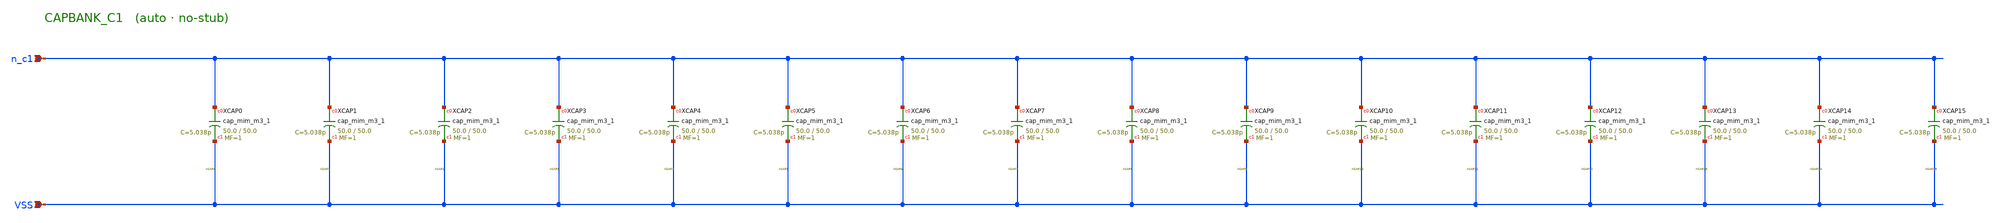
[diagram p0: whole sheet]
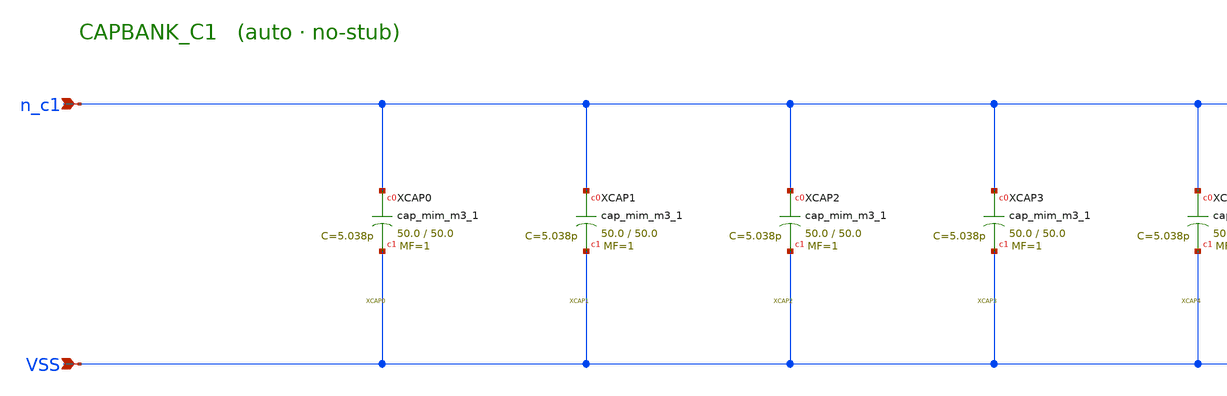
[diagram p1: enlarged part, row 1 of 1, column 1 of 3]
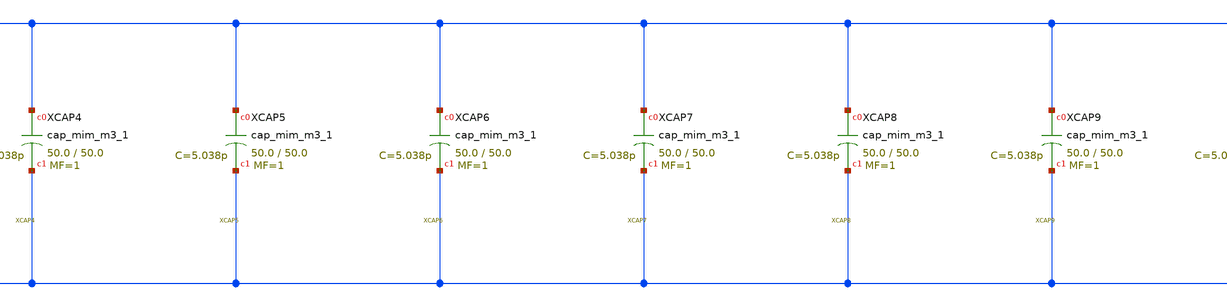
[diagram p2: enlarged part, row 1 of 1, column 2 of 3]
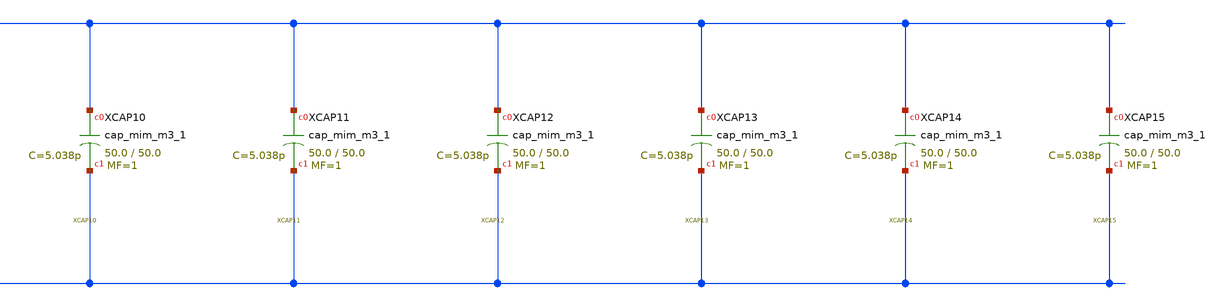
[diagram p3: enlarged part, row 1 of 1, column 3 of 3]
** sch_path: schematics/CAPBANK_C1.sch
**.subckt CAPBANK_C1 VSS n_c1
*.ipin VSS
*.ipin n_c1
XXCAP0 n_c1 VSS sky130_fd_pr__cap_mim_m3_1 W=50.0 L=50.0 MF=1 m=1
XXCAP1 n_c1 VSS sky130_fd_pr__cap_mim_m3_1 W=50.0 L=50.0 MF=1 m=1
XXCAP2 n_c1 VSS sky130_fd_pr__cap_mim_m3_1 W=50.0 L=50.0 MF=1 m=1
XXCAP3 n_c1 VSS sky130_fd_pr__cap_mim_m3_1 W=50.0 L=50.0 MF=1 m=1
XXCAP4 n_c1 VSS sky130_fd_pr__cap_mim_m3_1 W=50.0 L=50.0 MF=1 m=1
XXCAP5 n_c1 VSS sky130_fd_pr__cap_mim_m3_1 W=50.0 L=50.0 MF=1 m=1
XXCAP6 n_c1 VSS sky130_fd_pr__cap_mim_m3_1 W=50.0 L=50.0 MF=1 m=1
XXCAP7 n_c1 VSS sky130_fd_pr__cap_mim_m3_1 W=50.0 L=50.0 MF=1 m=1
XXCAP8 n_c1 VSS sky130_fd_pr__cap_mim_m3_1 W=50.0 L=50.0 MF=1 m=1
XXCAP9 n_c1 VSS sky130_fd_pr__cap_mim_m3_1 W=50.0 L=50.0 MF=1 m=1
XXCAP10 n_c1 VSS sky130_fd_pr__cap_mim_m3_1 W=50.0 L=50.0 MF=1 m=1
XXCAP11 n_c1 VSS sky130_fd_pr__cap_mim_m3_1 W=50.0 L=50.0 MF=1 m=1
XXCAP12 n_c1 VSS sky130_fd_pr__cap_mim_m3_1 W=50.0 L=50.0 MF=1 m=1
XXCAP13 n_c1 VSS sky130_fd_pr__cap_mim_m3_1 W=50.0 L=50.0 MF=1 m=1
XXCAP14 n_c1 VSS sky130_fd_pr__cap_mim_m3_1 W=50.0 L=50.0 MF=1 m=1
XXCAP15 n_c1 VSS sky130_fd_pr__cap_mim_m3_1 W=50.0 L=50.0 MF=1 m=1
**.ends
.end
